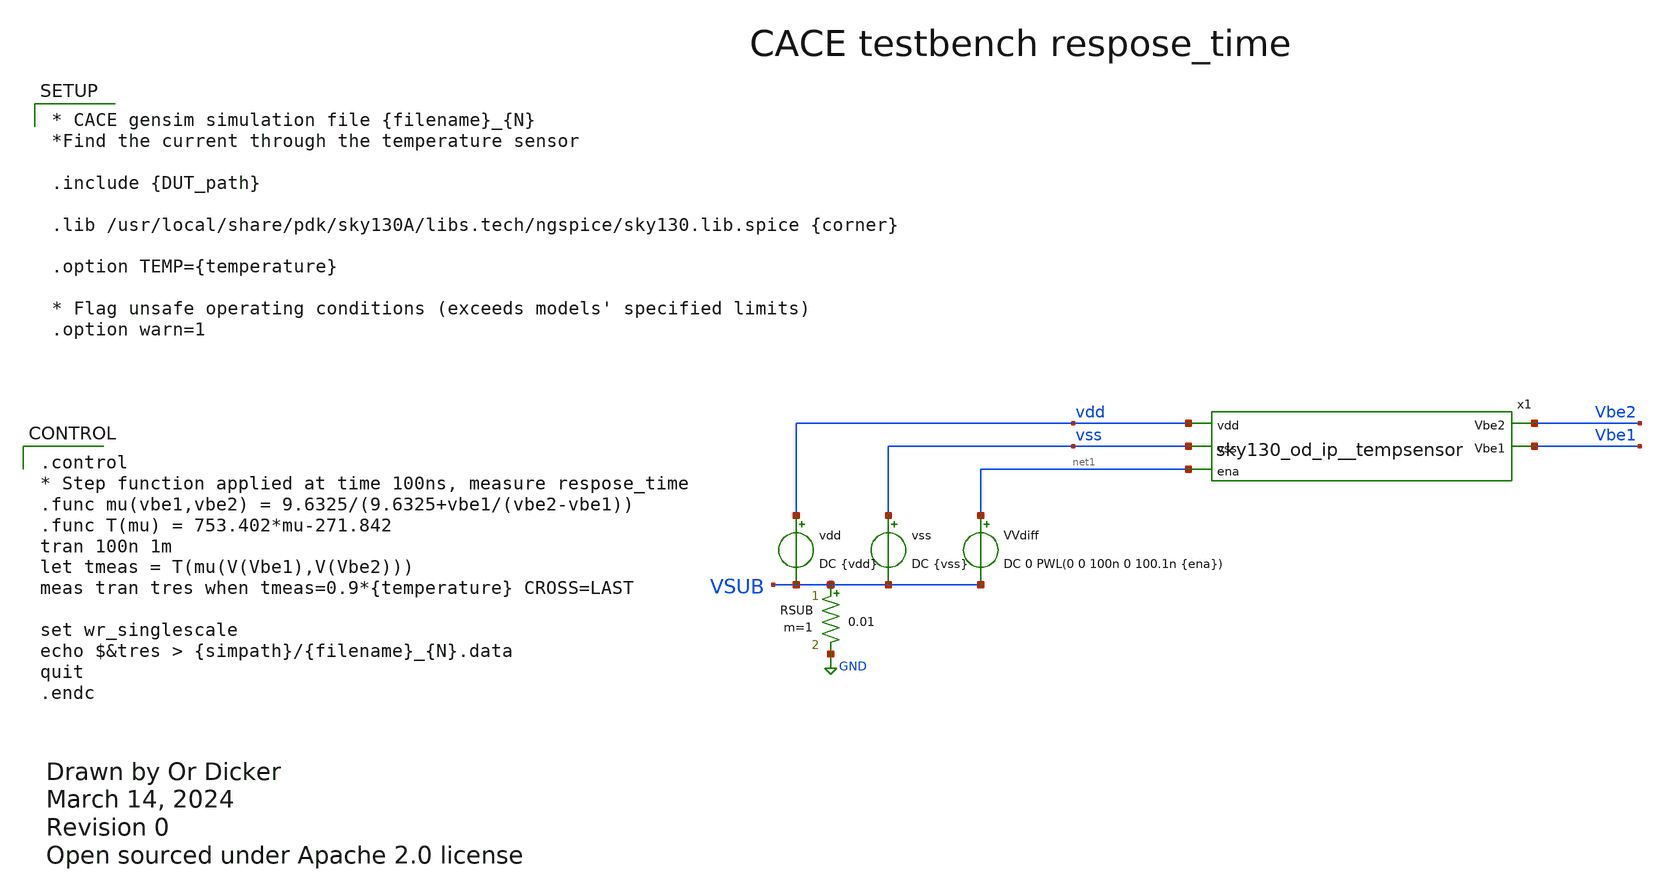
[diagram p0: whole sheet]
** sch_path: cace/respose_time.sch
* Open sourced under Apache 2.0 license
**.subckt respose_time
vss vss VSUB DC {vss}
vdd vdd VSUB DC {vdd}
RSUB VSUB GND 0.01 m=1
x1 vdd vss Vbe2 Vbe1 net1 sky130_od_ip__tempsensor
VVdiff net1 VSUB DC 0 PWL(0 0 100n 0 100.1n {ena})
**** begin user architecture code

.control
* Step function applied at time 100ns, measure respose_time
.func mu(vbe1,vbe2) = 9.6325/(9.6325+vbe1/(vbe2-vbe1))
.func T(mu) = 753.402*mu-271.842
tran 100n 1m
let tmeas = T(mu(V(Vbe1),V(Vbe2)))
meas tran tres when tmeas=0.9*{temperature} CROSS=LAST

set wr_singlescale
echo $&tres > {simpath}/{filename}_{N}.data
quit
.endc



* CACE gensim simulation file {filename}_{N}
*Find the current through the temperature sensor

.include {DUT_path}

.lib /usr/local/share/pdk/sky130A/libs.tech/ngspice/sky130.lib.spice {corner}

.option TEMP={temperature}

* Flag unsafe operating conditions (exceeds models' specified limits)
.option warn=1


**** end user architecture code
**.ends

* expanding   symbol:  xschem/sky130_od_ip__tempsensor.sym # of pins=5
** sym_path: xschem/sky130_od_ip__tempsensor.sym
** sch_path: xschem/sky130_od_ip__tempsensor.sch
.subckt sky130_od_ip__tempsensor vdd vss Vbe2 Vbe1 ena
*.ipin vdd
*.ipin vss
*.opin Vbe2
*.opin Vbe1
*.ipin ena
XM12 net1 Vp vdd vdd sky130_fd_pr__pfet_01v8 L=0.15 W=25 nf=1 ad='int((nf+1)/2) * W/nf * 0.29' as='int((nf+2)/2)
+ * W/nf * 0.29' pd='2*int((nf+1)/2) * (W/nf + 0.29)' ps='2*int((nf+2)/2) * (W/nf + 0.29)' nrd='0.29 /
+ W' nrs='0.29 / W' sa=0 sb=0 sd=0 mult=1 m=1
XM13 net2 Vp vdd vdd sky130_fd_pr__pfet_01v8 L=0.15 W=5 nf=1 ad='int((nf+1)/2) * W/nf * 0.29' as='int((nf+2)/2)
+ * W/nf * 0.29' pd='2*int((nf+1)/2) * (W/nf + 0.29)' ps='2*int((nf+2)/2) * (W/nf + 0.29)' nrd='0.29 /
+ W' nrs='0.29 / W' sa=0 sb=0 sd=0 mult=1 m=1
XQ_BR vss net3 net1 sky130_fd_pr__pnp_05v5_W3p40L3p40 m=1
XQ_BL vss vss net4 sky130_fd_pr__pnp_05v5_W3p40L3p40 m=1
Rb net2 net4 5k m=1
Rb_5 net3 vss 1k m=1
XM11 net5 Vp vdd vdd sky130_fd_pr__pfet_01v8 L=0.15 W=10 nf=1 ad='int((nf+1)/2) * W/nf * 0.29' as='int((nf+2)/2)
+ * W/nf * 0.29' pd='2*int((nf+1)/2) * (W/nf + 0.29)' ps='2*int((nf+2)/2) * (W/nf + 0.29)' nrd='0.29 /
+ W' nrs='0.29 / W' sa=0 sb=0 sd=0 mult=1 m=1
XM6 net6 net2 net5 vdd sky130_fd_pr__pfet_01v8 L=0.15 W=5 nf=1 ad='int((nf+1)/2) * W/nf * 0.29' as='int((nf+2)/2)
+ * W/nf * 0.29' pd='2*int((nf+1)/2) * (W/nf + 0.29)' ps='2*int((nf+2)/2) * (W/nf + 0.29)' nrd='0.29 /
+ W' nrs='0.29 / W' sa=0 sb=0 sd=0 mult=1 m=1
XM5 net7 net1 net5 vdd sky130_fd_pr__pfet_01v8 L=0.15 W=20 nf=1 ad='int((nf+1)/2) * W/nf * 0.29' as='int((nf+2)/2)
+ * W/nf * 0.29' pd='2*int((nf+1)/2) * (W/nf + 0.29)' ps='2*int((nf+2)/2) * (W/nf + 0.29)' nrd='0.29 /
+ W' nrs='0.29 / W' sa=0 sb=0 sd=0 mult=1 m=1
XM2 net6 net6 vss vss sky130_fd_pr__nfet_01v8 L=0.15 W=5 nf=1 ad='int((nf+1)/2) * W/nf * 0.29' as='int((nf+2)/2)
+ * W/nf * 0.29' pd='2*int((nf+1)/2) * (W/nf + 0.29)' ps='2*int((nf+2)/2) * (W/nf + 0.29)' nrd='0.29 /
+ W' nrs='0.29 / W' sa=0 sb=0 sd=0 mult=1 m=1
XM1 net7 net7 vss vss sky130_fd_pr__nfet_01v8 L=0.15 W=5 nf=1 ad='int((nf+1)/2) * W/nf * 0.29' as='int((nf+2)/2)
+ * W/nf * 0.29' pd='2*int((nf+1)/2) * (W/nf + 0.29)' ps='2*int((nf+2)/2) * (W/nf + 0.29)' nrd='0.29 /
+ W' nrs='0.29 / W' sa=0 sb=0 sd=0 mult=1 m=1
XM9 net8 Vp vdd vdd sky130_fd_pr__pfet_01v8 L=0.15 W=5 nf=1 ad='int((nf+1)/2) * W/nf * 0.29' as='int((nf+2)/2)
+ * W/nf * 0.29' pd='2*int((nf+1)/2) * (W/nf + 0.29)' ps='2*int((nf+2)/2) * (W/nf + 0.29)' nrd='0.29 /
+ W' nrs='0.29 / W' sa=0 sb=0 sd=0 mult=1 m=1
XM10 Vp Vp vdd vdd sky130_fd_pr__pfet_01v8 L=0.15 W=20 nf=1 ad='int((nf+1)/2) * W/nf * 0.29' as='int((nf+2)/2)
+ * W/nf * 0.29' pd='2*int((nf+1)/2) * (W/nf + 0.29)' ps='2*int((nf+2)/2) * (W/nf + 0.29)' nrd='0.29 /
+ W' nrs='0.29 / W' sa=0 sb=0 sd=0 mult=1 m=1
XM7 Vp net8 net10 vss sky130_fd_pr__nfet_01v8 L=0.15 W=5 nf=1 ad='int((nf+1)/2) * W/nf * 0.29' as='int((nf+2)/2)
+ * W/nf * 0.29' pd='2*int((nf+1)/2) * (W/nf + 0.29)' ps='2*int((nf+2)/2) * (W/nf + 0.29)' nrd='0.29 /
+ W' nrs='0.29 / W' sa=0 sb=0 sd=0 mult=1 m=1
XM8 net8 net8 net9 vss sky130_fd_pr__nfet_01v8 L=0.15 W=5 nf=1 ad='int((nf+1)/2) * W/nf * 0.29' as='int((nf+2)/2)
+ * W/nf * 0.29' pd='2*int((nf+1)/2) * (W/nf + 0.29)' ps='2*int((nf+2)/2) * (W/nf + 0.29)' nrd='0.29 /
+ W' nrs='0.29 / W' sa=0 sb=0 sd=0 mult=1 m=1
XM3 net10 net6 vss vss sky130_fd_pr__nfet_01v8 L=0.15 W=5 nf=1 ad='int((nf+1)/2) * W/nf * 0.29' as='int((nf+2)/2)
+ * W/nf * 0.29' pd='2*int((nf+1)/2) * (W/nf + 0.29)' ps='2*int((nf+2)/2) * (W/nf + 0.29)' nrd='0.29 /
+ W' nrs='0.29 / W' sa=0 sb=0 sd=0 mult=1 m=1
XM4 net9 net9 vss vss sky130_fd_pr__nfet_01v8 L=0.15 W=5 nf=1 ad='int((nf+1)/2) * W/nf * 0.29' as='int((nf+2)/2)
+ * W/nf * 0.29' pd='2*int((nf+1)/2) * (W/nf + 0.29)' ps='2*int((nf+2)/2) * (W/nf + 0.29)' nrd='0.29 /
+ W' nrs='0.29 / W' sa=0 sb=0 sd=0 mult=1 m=1
XQ_BL1 vss vss Vbe1 sky130_fd_pr__pnp_05v5_W3p40L3p40 m=1
XQ_BR1 vss vss Vbe2 sky130_fd_pr__pnp_05v5_W3p40L3p40 m=1
XM14 Vbe1 Vp vdd vdd sky130_fd_pr__pfet_01v8 L=0.15 W=10 nf=1 ad='int((nf+1)/2) * W/nf * 0.29' as='int((nf+2)/2)
+ * W/nf * 0.29' pd='2*int((nf+1)/2) * (W/nf + 0.29)' ps='2*int((nf+2)/2) * (W/nf + 0.29)' nrd='0.29 /
+ W' nrs='0.29 / W' sa=0 sb=0 sd=0 mult=1 m=1
XM15 Vbe2 Vp vdd vdd sky130_fd_pr__pfet_01v8 L=0.15 W=50 nf=1 ad='int((nf+1)/2) * W/nf * 0.29' as='int((nf+2)/2)
+ * W/nf * 0.29' pd='2*int((nf+1)/2) * (W/nf + 0.29)' ps='2*int((nf+2)/2) * (W/nf + 0.29)' nrd='0.29 /
+ W' nrs='0.29 / W' sa=0 sb=0 sd=0 mult=1 m=1
XM16 Vp ena vdd vdd sky130_fd_pr__pfet_01v8 L=0.15 W=1 nf=1 ad='int((nf+1)/2) * W/nf * 0.29' as='int((nf+2)/2)
+ * W/nf * 0.29' pd='2*int((nf+1)/2) * (W/nf + 0.29)' ps='2*int((nf+2)/2) * (W/nf + 0.29)' nrd='0.29 /
+ W' nrs='0.29 / W' sa=0 sb=0 sd=0 mult=1 m=1
.ends

.GLOBAL GND
.end
